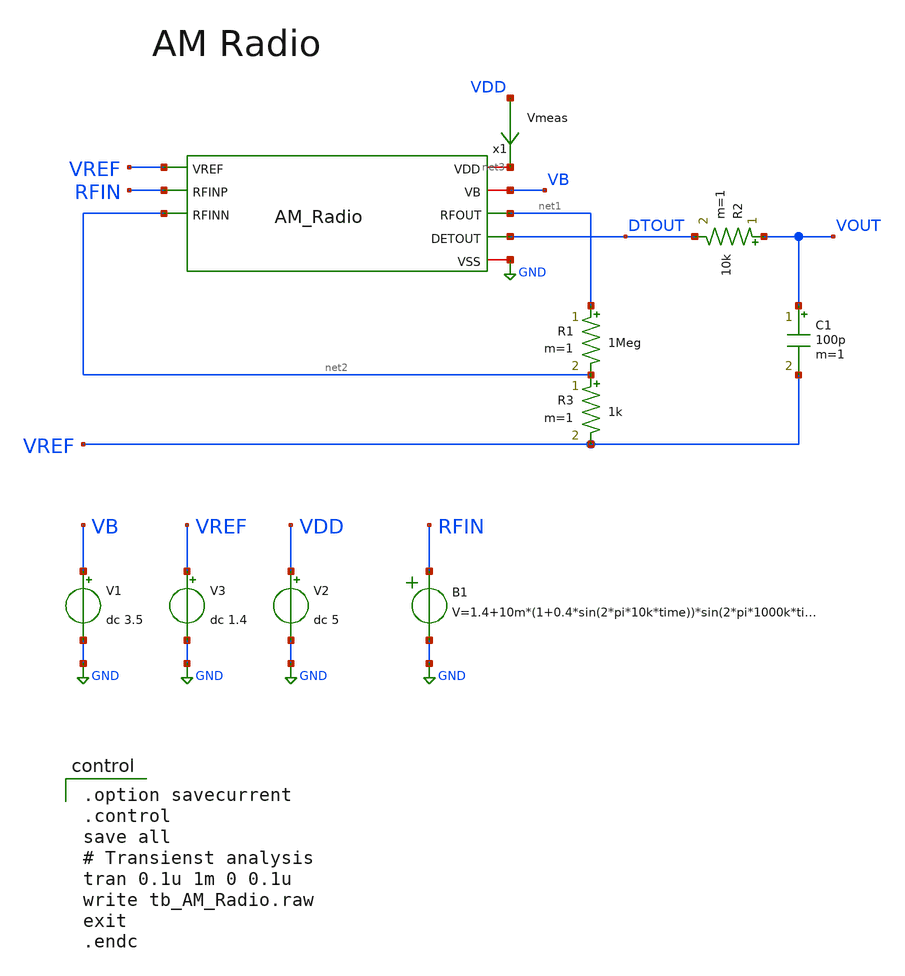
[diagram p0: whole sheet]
** sch_path: member_project/AM_Radio/noritsuna/xschem/tb_am_radio.sch
**.subckt tb_am_radio
V2 VDD GND dc 5
V3 VREF GND dc 1.4
B1 RFIN GND V=1.4+10m*(1+0.4*sin(2*pi*10k*time))*sin(2*pi*1000k*time)
R2 VOUT DTOUT 10k m=1
C1 VOUT VREF 100p m=1
x1 net3 VB VREF RFIN net2 DTOUT GND net1 AM_Radio
R1 net1 net2 1Meg m=1
Vmeas VDD net3 0
.save i(vmeas)
R3 net2 VREF 1k m=1
V1 VB GND dc 3.5
**** begin user architecture code
 .include $::LIB/ip62_models

.option savecurrent
.control
save all
# Transienst analysis
tran 0.1u 1m 0 0.1u
write tb_AM_Radio.raw
exit
.endc

**** end user architecture code
**.ends
.GLOBAL GND
.end
